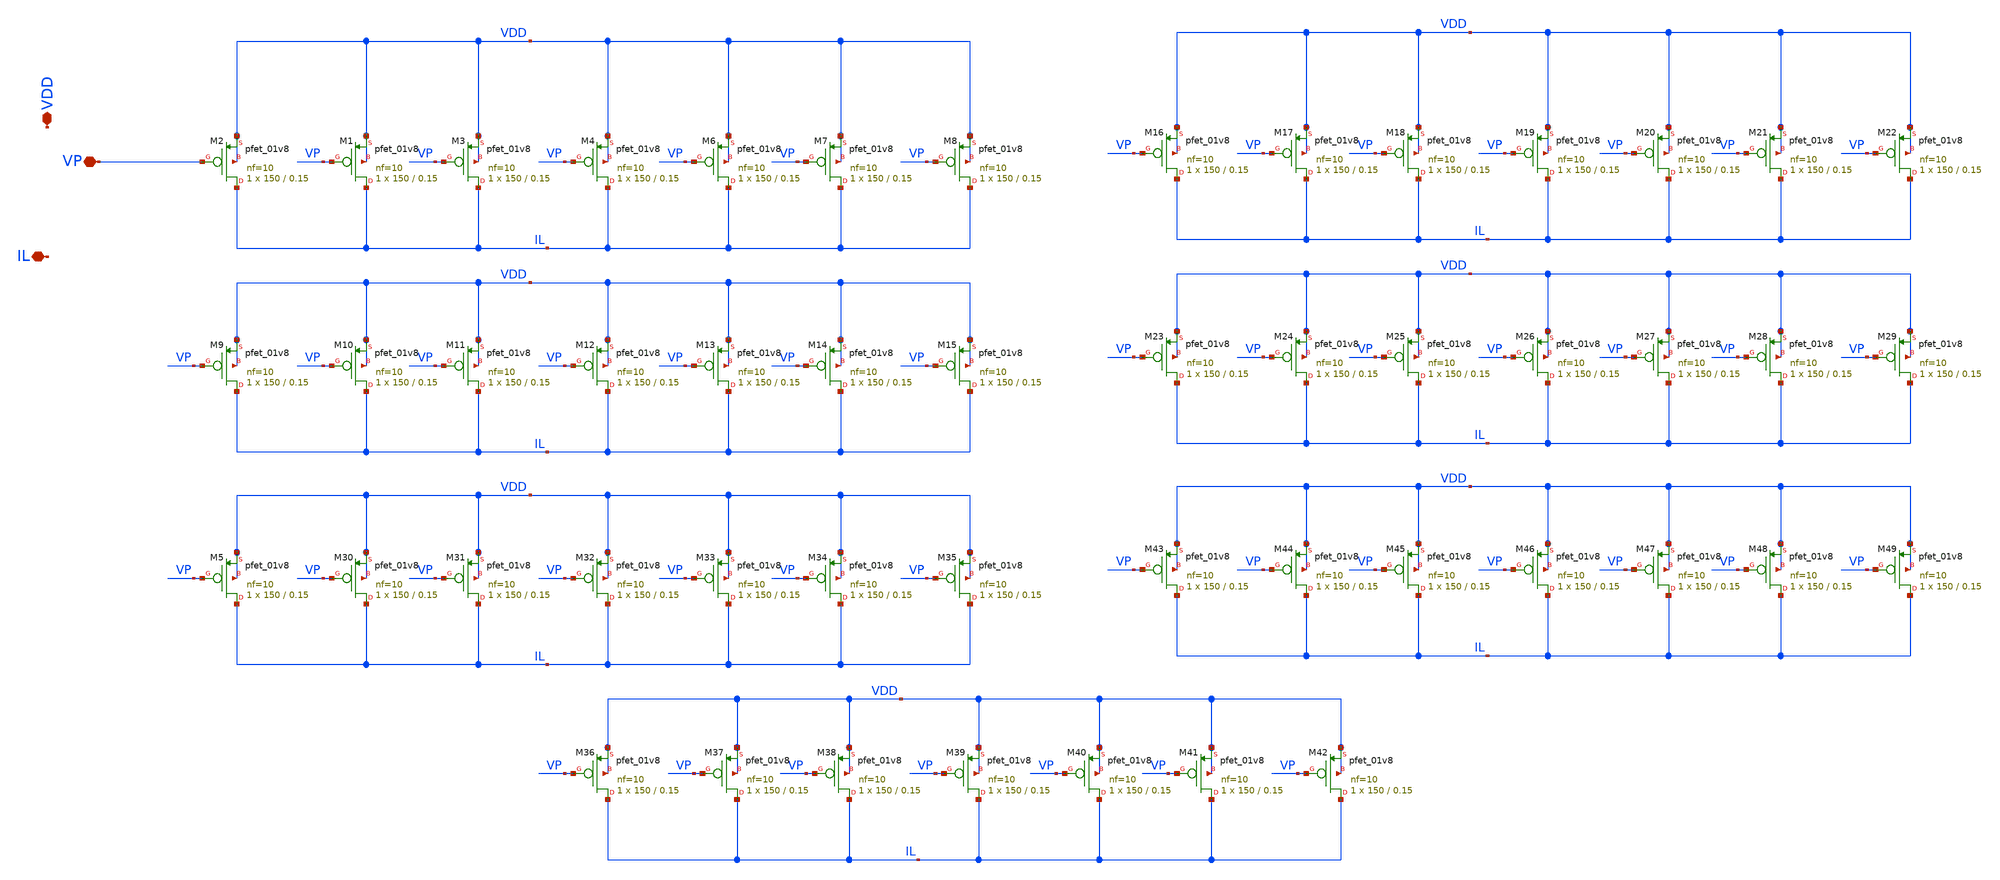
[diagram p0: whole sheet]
** sch_path: xschem/DC_DC_Converter_xschem/DC_DC_Converter/Power_Mosfet/P_Power_mosfets.sch
**.subckt P_Power_mosfets VDD VP IL
*.iopin VDD
*.iopin VP
*.iopin IL
XM2 IL VP VDD VDD sky130_fd_pr__pfet_01v8 L=0.15 W=150 nf=10 ad='int((nf+1)/2) * W/nf * 0.29' as='int((nf+2)/2) * W/nf * 0.29'
+ pd='2*int((nf+1)/2) * (W/nf + 0.29)' ps='2*int((nf+2)/2) * (W/nf + 0.29)' nrd='0.29 / W' nrs='0.29 / W'
+ sa=0 sb=0 sd=0 mult=1 m=1
XM1 IL VP VDD VDD sky130_fd_pr__pfet_01v8 L=0.15 W=150 nf=10 ad='int((nf+1)/2) * W/nf * 0.29' as='int((nf+2)/2) * W/nf * 0.29'
+ pd='2*int((nf+1)/2) * (W/nf + 0.29)' ps='2*int((nf+2)/2) * (W/nf + 0.29)' nrd='0.29 / W' nrs='0.29 / W'
+ sa=0 sb=0 sd=0 mult=1 m=1
XM3 IL VP VDD VDD sky130_fd_pr__pfet_01v8 L=0.15 W=150 nf=10 ad='int((nf+1)/2) * W/nf * 0.29' as='int((nf+2)/2) * W/nf * 0.29'
+ pd='2*int((nf+1)/2) * (W/nf + 0.29)' ps='2*int((nf+2)/2) * (W/nf + 0.29)' nrd='0.29 / W' nrs='0.29 / W'
+ sa=0 sb=0 sd=0 mult=1 m=1
XM4 IL VP VDD VDD sky130_fd_pr__pfet_01v8 L=0.15 W=150 nf=10 ad='int((nf+1)/2) * W/nf * 0.29' as='int((nf+2)/2) * W/nf * 0.29'
+ pd='2*int((nf+1)/2) * (W/nf + 0.29)' ps='2*int((nf+2)/2) * (W/nf + 0.29)' nrd='0.29 / W' nrs='0.29 / W'
+ sa=0 sb=0 sd=0 mult=1 m=1
XM6 IL VP VDD VDD sky130_fd_pr__pfet_01v8 L=0.15 W=150 nf=10 ad='int((nf+1)/2) * W/nf * 0.29' as='int((nf+2)/2) * W/nf * 0.29'
+ pd='2*int((nf+1)/2) * (W/nf + 0.29)' ps='2*int((nf+2)/2) * (W/nf + 0.29)' nrd='0.29 / W' nrs='0.29 / W'
+ sa=0 sb=0 sd=0 mult=1 m=1
XM7 IL VP VDD VDD sky130_fd_pr__pfet_01v8 L=0.15 W=150 nf=10 ad='int((nf+1)/2) * W/nf * 0.29' as='int((nf+2)/2) * W/nf * 0.29'
+ pd='2*int((nf+1)/2) * (W/nf + 0.29)' ps='2*int((nf+2)/2) * (W/nf + 0.29)' nrd='0.29 / W' nrs='0.29 / W'
+ sa=0 sb=0 sd=0 mult=1 m=1
XM8 IL VP VDD VDD sky130_fd_pr__pfet_01v8 L=0.15 W=150 nf=10 ad='int((nf+1)/2) * W/nf * 0.29' as='int((nf+2)/2) * W/nf * 0.29'
+ pd='2*int((nf+1)/2) * (W/nf + 0.29)' ps='2*int((nf+2)/2) * (W/nf + 0.29)' nrd='0.29 / W' nrs='0.29 / W'
+ sa=0 sb=0 sd=0 mult=1 m=1
XM9 IL VP VDD VDD sky130_fd_pr__pfet_01v8 L=0.15 W=150 nf=10 ad='int((nf+1)/2) * W/nf * 0.29' as='int((nf+2)/2) * W/nf * 0.29'
+ pd='2*int((nf+1)/2) * (W/nf + 0.29)' ps='2*int((nf+2)/2) * (W/nf + 0.29)' nrd='0.29 / W' nrs='0.29 / W'
+ sa=0 sb=0 sd=0 mult=1 m=1
XM10 IL VP VDD VDD sky130_fd_pr__pfet_01v8 L=0.15 W=150 nf=10 ad='int((nf+1)/2) * W/nf * 0.29' as='int((nf+2)/2) * W/nf * 0.29'
+ pd='2*int((nf+1)/2) * (W/nf + 0.29)' ps='2*int((nf+2)/2) * (W/nf + 0.29)' nrd='0.29 / W' nrs='0.29 / W'
+ sa=0 sb=0 sd=0 mult=1 m=1
XM11 IL VP VDD VDD sky130_fd_pr__pfet_01v8 L=0.15 W=150 nf=10 ad='int((nf+1)/2) * W/nf * 0.29' as='int((nf+2)/2) * W/nf * 0.29'
+ pd='2*int((nf+1)/2) * (W/nf + 0.29)' ps='2*int((nf+2)/2) * (W/nf + 0.29)' nrd='0.29 / W' nrs='0.29 / W'
+ sa=0 sb=0 sd=0 mult=1 m=1
XM12 IL VP VDD VDD sky130_fd_pr__pfet_01v8 L=0.15 W=150 nf=10 ad='int((nf+1)/2) * W/nf * 0.29' as='int((nf+2)/2) * W/nf * 0.29'
+ pd='2*int((nf+1)/2) * (W/nf + 0.29)' ps='2*int((nf+2)/2) * (W/nf + 0.29)' nrd='0.29 / W' nrs='0.29 / W'
+ sa=0 sb=0 sd=0 mult=1 m=1
XM13 IL VP VDD VDD sky130_fd_pr__pfet_01v8 L=0.15 W=150 nf=10 ad='int((nf+1)/2) * W/nf * 0.29' as='int((nf+2)/2) * W/nf * 0.29'
+ pd='2*int((nf+1)/2) * (W/nf + 0.29)' ps='2*int((nf+2)/2) * (W/nf + 0.29)' nrd='0.29 / W' nrs='0.29 / W'
+ sa=0 sb=0 sd=0 mult=1 m=1
XM14 IL VP VDD VDD sky130_fd_pr__pfet_01v8 L=0.15 W=150 nf=10 ad='int((nf+1)/2) * W/nf * 0.29' as='int((nf+2)/2) * W/nf * 0.29'
+ pd='2*int((nf+1)/2) * (W/nf + 0.29)' ps='2*int((nf+2)/2) * (W/nf + 0.29)' nrd='0.29 / W' nrs='0.29 / W'
+ sa=0 sb=0 sd=0 mult=1 m=1
XM15 IL VP VDD VDD sky130_fd_pr__pfet_01v8 L=0.15 W=150 nf=10 ad='int((nf+1)/2) * W/nf * 0.29' as='int((nf+2)/2) * W/nf * 0.29'
+ pd='2*int((nf+1)/2) * (W/nf + 0.29)' ps='2*int((nf+2)/2) * (W/nf + 0.29)' nrd='0.29 / W' nrs='0.29 / W'
+ sa=0 sb=0 sd=0 mult=1 m=1
XM16 IL VP VDD VDD sky130_fd_pr__pfet_01v8 L=0.15 W=150 nf=10 ad='int((nf+1)/2) * W/nf * 0.29' as='int((nf+2)/2) * W/nf * 0.29'
+ pd='2*int((nf+1)/2) * (W/nf + 0.29)' ps='2*int((nf+2)/2) * (W/nf + 0.29)' nrd='0.29 / W' nrs='0.29 / W'
+ sa=0 sb=0 sd=0 mult=1 m=1
XM17 IL VP VDD VDD sky130_fd_pr__pfet_01v8 L=0.15 W=150 nf=10 ad='int((nf+1)/2) * W/nf * 0.29' as='int((nf+2)/2) * W/nf * 0.29'
+ pd='2*int((nf+1)/2) * (W/nf + 0.29)' ps='2*int((nf+2)/2) * (W/nf + 0.29)' nrd='0.29 / W' nrs='0.29 / W'
+ sa=0 sb=0 sd=0 mult=1 m=1
XM18 IL VP VDD VDD sky130_fd_pr__pfet_01v8 L=0.15 W=150 nf=10 ad='int((nf+1)/2) * W/nf * 0.29' as='int((nf+2)/2) * W/nf * 0.29'
+ pd='2*int((nf+1)/2) * (W/nf + 0.29)' ps='2*int((nf+2)/2) * (W/nf + 0.29)' nrd='0.29 / W' nrs='0.29 / W'
+ sa=0 sb=0 sd=0 mult=1 m=1
XM19 IL VP VDD VDD sky130_fd_pr__pfet_01v8 L=0.15 W=150 nf=10 ad='int((nf+1)/2) * W/nf * 0.29' as='int((nf+2)/2) * W/nf * 0.29'
+ pd='2*int((nf+1)/2) * (W/nf + 0.29)' ps='2*int((nf+2)/2) * (W/nf + 0.29)' nrd='0.29 / W' nrs='0.29 / W'
+ sa=0 sb=0 sd=0 mult=1 m=1
XM20 IL VP VDD VDD sky130_fd_pr__pfet_01v8 L=0.15 W=150 nf=10 ad='int((nf+1)/2) * W/nf * 0.29' as='int((nf+2)/2) * W/nf * 0.29'
+ pd='2*int((nf+1)/2) * (W/nf + 0.29)' ps='2*int((nf+2)/2) * (W/nf + 0.29)' nrd='0.29 / W' nrs='0.29 / W'
+ sa=0 sb=0 sd=0 mult=1 m=1
XM21 IL VP VDD VDD sky130_fd_pr__pfet_01v8 L=0.15 W=150 nf=10 ad='int((nf+1)/2) * W/nf * 0.29' as='int((nf+2)/2) * W/nf * 0.29'
+ pd='2*int((nf+1)/2) * (W/nf + 0.29)' ps='2*int((nf+2)/2) * (W/nf + 0.29)' nrd='0.29 / W' nrs='0.29 / W'
+ sa=0 sb=0 sd=0 mult=1 m=1
XM22 IL VP VDD VDD sky130_fd_pr__pfet_01v8 L=0.15 W=150 nf=10 ad='int((nf+1)/2) * W/nf * 0.29' as='int((nf+2)/2) * W/nf * 0.29'
+ pd='2*int((nf+1)/2) * (W/nf + 0.29)' ps='2*int((nf+2)/2) * (W/nf + 0.29)' nrd='0.29 / W' nrs='0.29 / W'
+ sa=0 sb=0 sd=0 mult=1 m=1
XM23 IL VP VDD VDD sky130_fd_pr__pfet_01v8 L=0.15 W=150 nf=10 ad='int((nf+1)/2) * W/nf * 0.29' as='int((nf+2)/2) * W/nf * 0.29'
+ pd='2*int((nf+1)/2) * (W/nf + 0.29)' ps='2*int((nf+2)/2) * (W/nf + 0.29)' nrd='0.29 / W' nrs='0.29 / W'
+ sa=0 sb=0 sd=0 mult=1 m=1
XM24 IL VP VDD VDD sky130_fd_pr__pfet_01v8 L=0.15 W=150 nf=10 ad='int((nf+1)/2) * W/nf * 0.29' as='int((nf+2)/2) * W/nf * 0.29'
+ pd='2*int((nf+1)/2) * (W/nf + 0.29)' ps='2*int((nf+2)/2) * (W/nf + 0.29)' nrd='0.29 / W' nrs='0.29 / W'
+ sa=0 sb=0 sd=0 mult=1 m=1
XM25 IL VP VDD VDD sky130_fd_pr__pfet_01v8 L=0.15 W=150 nf=10 ad='int((nf+1)/2) * W/nf * 0.29' as='int((nf+2)/2) * W/nf * 0.29'
+ pd='2*int((nf+1)/2) * (W/nf + 0.29)' ps='2*int((nf+2)/2) * (W/nf + 0.29)' nrd='0.29 / W' nrs='0.29 / W'
+ sa=0 sb=0 sd=0 mult=1 m=1
XM26 IL VP VDD VDD sky130_fd_pr__pfet_01v8 L=0.15 W=150 nf=10 ad='int((nf+1)/2) * W/nf * 0.29' as='int((nf+2)/2) * W/nf * 0.29'
+ pd='2*int((nf+1)/2) * (W/nf + 0.29)' ps='2*int((nf+2)/2) * (W/nf + 0.29)' nrd='0.29 / W' nrs='0.29 / W'
+ sa=0 sb=0 sd=0 mult=1 m=1
XM27 IL VP VDD VDD sky130_fd_pr__pfet_01v8 L=0.15 W=150 nf=10 ad='int((nf+1)/2) * W/nf * 0.29' as='int((nf+2)/2) * W/nf * 0.29'
+ pd='2*int((nf+1)/2) * (W/nf + 0.29)' ps='2*int((nf+2)/2) * (W/nf + 0.29)' nrd='0.29 / W' nrs='0.29 / W'
+ sa=0 sb=0 sd=0 mult=1 m=1
XM28 IL VP VDD VDD sky130_fd_pr__pfet_01v8 L=0.15 W=150 nf=10 ad='int((nf+1)/2) * W/nf * 0.29' as='int((nf+2)/2) * W/nf * 0.29'
+ pd='2*int((nf+1)/2) * (W/nf + 0.29)' ps='2*int((nf+2)/2) * (W/nf + 0.29)' nrd='0.29 / W' nrs='0.29 / W'
+ sa=0 sb=0 sd=0 mult=1 m=1
XM29 IL VP VDD VDD sky130_fd_pr__pfet_01v8 L=0.15 W=150 nf=10 ad='int((nf+1)/2) * W/nf * 0.29' as='int((nf+2)/2) * W/nf * 0.29'
+ pd='2*int((nf+1)/2) * (W/nf + 0.29)' ps='2*int((nf+2)/2) * (W/nf + 0.29)' nrd='0.29 / W' nrs='0.29 / W'
+ sa=0 sb=0 sd=0 mult=1 m=1
XM5 IL VP VDD VDD sky130_fd_pr__pfet_01v8 L=0.15 W=150 nf=10 ad='int((nf+1)/2) * W/nf * 0.29' as='int((nf+2)/2) * W/nf * 0.29'
+ pd='2*int((nf+1)/2) * (W/nf + 0.29)' ps='2*int((nf+2)/2) * (W/nf + 0.29)' nrd='0.29 / W' nrs='0.29 / W'
+ sa=0 sb=0 sd=0 mult=1 m=1
XM30 IL VP VDD VDD sky130_fd_pr__pfet_01v8 L=0.15 W=150 nf=10 ad='int((nf+1)/2) * W/nf * 0.29' as='int((nf+2)/2) * W/nf * 0.29'
+ pd='2*int((nf+1)/2) * (W/nf + 0.29)' ps='2*int((nf+2)/2) * (W/nf + 0.29)' nrd='0.29 / W' nrs='0.29 / W'
+ sa=0 sb=0 sd=0 mult=1 m=1
XM31 IL VP VDD VDD sky130_fd_pr__pfet_01v8 L=0.15 W=150 nf=10 ad='int((nf+1)/2) * W/nf * 0.29' as='int((nf+2)/2) * W/nf * 0.29'
+ pd='2*int((nf+1)/2) * (W/nf + 0.29)' ps='2*int((nf+2)/2) * (W/nf + 0.29)' nrd='0.29 / W' nrs='0.29 / W'
+ sa=0 sb=0 sd=0 mult=1 m=1
XM32 IL VP VDD VDD sky130_fd_pr__pfet_01v8 L=0.15 W=150 nf=10 ad='int((nf+1)/2) * W/nf * 0.29' as='int((nf+2)/2) * W/nf * 0.29'
+ pd='2*int((nf+1)/2) * (W/nf + 0.29)' ps='2*int((nf+2)/2) * (W/nf + 0.29)' nrd='0.29 / W' nrs='0.29 / W'
+ sa=0 sb=0 sd=0 mult=1 m=1
XM33 IL VP VDD VDD sky130_fd_pr__pfet_01v8 L=0.15 W=150 nf=10 ad='int((nf+1)/2) * W/nf * 0.29' as='int((nf+2)/2) * W/nf * 0.29'
+ pd='2*int((nf+1)/2) * (W/nf + 0.29)' ps='2*int((nf+2)/2) * (W/nf + 0.29)' nrd='0.29 / W' nrs='0.29 / W'
+ sa=0 sb=0 sd=0 mult=1 m=1
XM34 IL VP VDD VDD sky130_fd_pr__pfet_01v8 L=0.15 W=150 nf=10 ad='int((nf+1)/2) * W/nf * 0.29' as='int((nf+2)/2) * W/nf * 0.29'
+ pd='2*int((nf+1)/2) * (W/nf + 0.29)' ps='2*int((nf+2)/2) * (W/nf + 0.29)' nrd='0.29 / W' nrs='0.29 / W'
+ sa=0 sb=0 sd=0 mult=1 m=1
XM35 IL VP VDD VDD sky130_fd_pr__pfet_01v8 L=0.15 W=150 nf=10 ad='int((nf+1)/2) * W/nf * 0.29' as='int((nf+2)/2) * W/nf * 0.29'
+ pd='2*int((nf+1)/2) * (W/nf + 0.29)' ps='2*int((nf+2)/2) * (W/nf + 0.29)' nrd='0.29 / W' nrs='0.29 / W'
+ sa=0 sb=0 sd=0 mult=1 m=1
XM36 IL VP VDD VDD sky130_fd_pr__pfet_01v8 L=0.15 W=150 nf=10 ad='int((nf+1)/2) * W/nf * 0.29' as='int((nf+2)/2) * W/nf * 0.29'
+ pd='2*int((nf+1)/2) * (W/nf + 0.29)' ps='2*int((nf+2)/2) * (W/nf + 0.29)' nrd='0.29 / W' nrs='0.29 / W'
+ sa=0 sb=0 sd=0 mult=1 m=1
XM37 IL VP VDD VDD sky130_fd_pr__pfet_01v8 L=0.15 W=150 nf=10 ad='int((nf+1)/2) * W/nf * 0.29' as='int((nf+2)/2) * W/nf * 0.29'
+ pd='2*int((nf+1)/2) * (W/nf + 0.29)' ps='2*int((nf+2)/2) * (W/nf + 0.29)' nrd='0.29 / W' nrs='0.29 / W'
+ sa=0 sb=0 sd=0 mult=1 m=1
XM38 IL VP VDD VDD sky130_fd_pr__pfet_01v8 L=0.15 W=150 nf=10 ad='int((nf+1)/2) * W/nf * 0.29' as='int((nf+2)/2) * W/nf * 0.29'
+ pd='2*int((nf+1)/2) * (W/nf + 0.29)' ps='2*int((nf+2)/2) * (W/nf + 0.29)' nrd='0.29 / W' nrs='0.29 / W'
+ sa=0 sb=0 sd=0 mult=1 m=1
XM39 IL VP VDD VDD sky130_fd_pr__pfet_01v8 L=0.15 W=150 nf=10 ad='int((nf+1)/2) * W/nf * 0.29' as='int((nf+2)/2) * W/nf * 0.29'
+ pd='2*int((nf+1)/2) * (W/nf + 0.29)' ps='2*int((nf+2)/2) * (W/nf + 0.29)' nrd='0.29 / W' nrs='0.29 / W'
+ sa=0 sb=0 sd=0 mult=1 m=1
XM40 IL VP VDD VDD sky130_fd_pr__pfet_01v8 L=0.15 W=150 nf=10 ad='int((nf+1)/2) * W/nf * 0.29' as='int((nf+2)/2) * W/nf * 0.29'
+ pd='2*int((nf+1)/2) * (W/nf + 0.29)' ps='2*int((nf+2)/2) * (W/nf + 0.29)' nrd='0.29 / W' nrs='0.29 / W'
+ sa=0 sb=0 sd=0 mult=1 m=1
XM41 IL VP VDD VDD sky130_fd_pr__pfet_01v8 L=0.15 W=150 nf=10 ad='int((nf+1)/2) * W/nf * 0.29' as='int((nf+2)/2) * W/nf * 0.29'
+ pd='2*int((nf+1)/2) * (W/nf + 0.29)' ps='2*int((nf+2)/2) * (W/nf + 0.29)' nrd='0.29 / W' nrs='0.29 / W'
+ sa=0 sb=0 sd=0 mult=1 m=1
XM42 IL VP VDD VDD sky130_fd_pr__pfet_01v8 L=0.15 W=150 nf=10 ad='int((nf+1)/2) * W/nf * 0.29' as='int((nf+2)/2) * W/nf * 0.29'
+ pd='2*int((nf+1)/2) * (W/nf + 0.29)' ps='2*int((nf+2)/2) * (W/nf + 0.29)' nrd='0.29 / W' nrs='0.29 / W'
+ sa=0 sb=0 sd=0 mult=1 m=1
XM43 IL VP VDD VDD sky130_fd_pr__pfet_01v8 L=0.15 W=150 nf=10 ad='int((nf+1)/2) * W/nf * 0.29' as='int((nf+2)/2) * W/nf * 0.29'
+ pd='2*int((nf+1)/2) * (W/nf + 0.29)' ps='2*int((nf+2)/2) * (W/nf + 0.29)' nrd='0.29 / W' nrs='0.29 / W'
+ sa=0 sb=0 sd=0 mult=1 m=1
XM44 IL VP VDD VDD sky130_fd_pr__pfet_01v8 L=0.15 W=150 nf=10 ad='int((nf+1)/2) * W/nf * 0.29' as='int((nf+2)/2) * W/nf * 0.29'
+ pd='2*int((nf+1)/2) * (W/nf + 0.29)' ps='2*int((nf+2)/2) * (W/nf + 0.29)' nrd='0.29 / W' nrs='0.29 / W'
+ sa=0 sb=0 sd=0 mult=1 m=1
XM45 IL VP VDD VDD sky130_fd_pr__pfet_01v8 L=0.15 W=150 nf=10 ad='int((nf+1)/2) * W/nf * 0.29' as='int((nf+2)/2) * W/nf * 0.29'
+ pd='2*int((nf+1)/2) * (W/nf + 0.29)' ps='2*int((nf+2)/2) * (W/nf + 0.29)' nrd='0.29 / W' nrs='0.29 / W'
+ sa=0 sb=0 sd=0 mult=1 m=1
XM46 IL VP VDD VDD sky130_fd_pr__pfet_01v8 L=0.15 W=150 nf=10 ad='int((nf+1)/2) * W/nf * 0.29' as='int((nf+2)/2) * W/nf * 0.29'
+ pd='2*int((nf+1)/2) * (W/nf + 0.29)' ps='2*int((nf+2)/2) * (W/nf + 0.29)' nrd='0.29 / W' nrs='0.29 / W'
+ sa=0 sb=0 sd=0 mult=1 m=1
XM47 IL VP VDD VDD sky130_fd_pr__pfet_01v8 L=0.15 W=150 nf=10 ad='int((nf+1)/2) * W/nf * 0.29' as='int((nf+2)/2) * W/nf * 0.29'
+ pd='2*int((nf+1)/2) * (W/nf + 0.29)' ps='2*int((nf+2)/2) * (W/nf + 0.29)' nrd='0.29 / W' nrs='0.29 / W'
+ sa=0 sb=0 sd=0 mult=1 m=1
XM48 IL VP VDD VDD sky130_fd_pr__pfet_01v8 L=0.15 W=150 nf=10 ad='int((nf+1)/2) * W/nf * 0.29' as='int((nf+2)/2) * W/nf * 0.29'
+ pd='2*int((nf+1)/2) * (W/nf + 0.29)' ps='2*int((nf+2)/2) * (W/nf + 0.29)' nrd='0.29 / W' nrs='0.29 / W'
+ sa=0 sb=0 sd=0 mult=1 m=1
XM49 IL VP VDD VDD sky130_fd_pr__pfet_01v8 L=0.15 W=150 nf=10 ad='int((nf+1)/2) * W/nf * 0.29' as='int((nf+2)/2) * W/nf * 0.29'
+ pd='2*int((nf+1)/2) * (W/nf + 0.29)' ps='2*int((nf+2)/2) * (W/nf + 0.29)' nrd='0.29 / W' nrs='0.29 / W'
+ sa=0 sb=0 sd=0 mult=1 m=1
**.ends
.end
